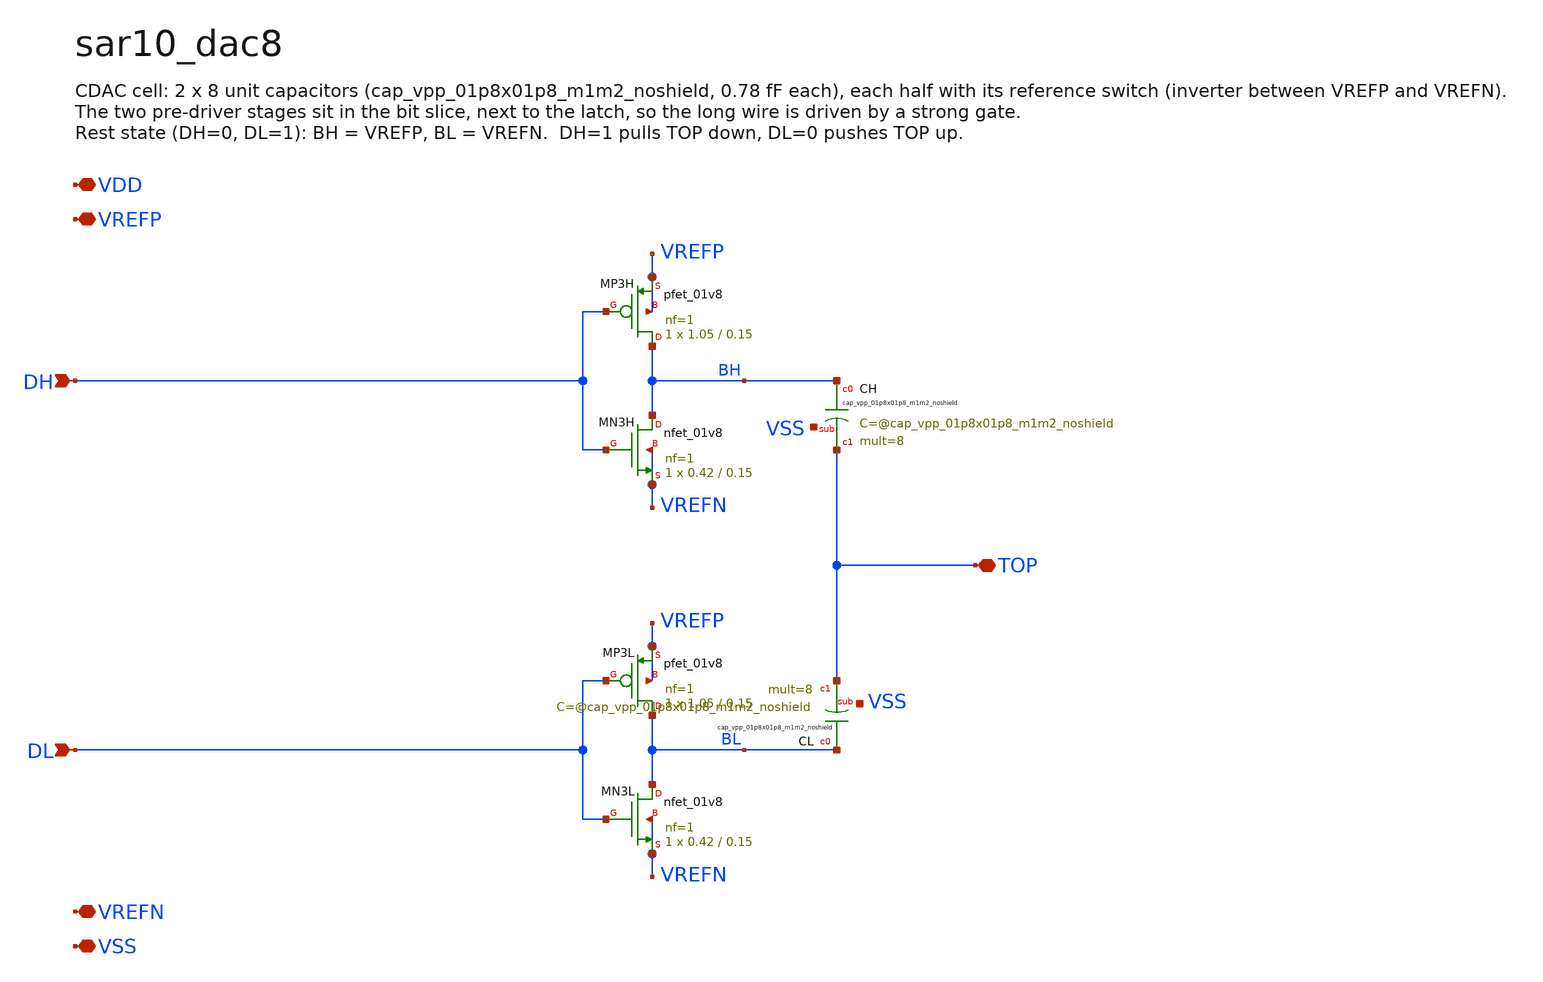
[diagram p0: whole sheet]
** sch_path: xschem/sar10_dac8.sch
**.subckt sar10_dac8 DH DL TOP VDD VREFP VREFN VSS
*.ipin DH
*.ipin DL
*.iopin TOP
*.iopin VDD
*.iopin VREFP
*.iopin VREFN
*.iopin VSS
XMP3H BH DH VREFP VREFP sky130_fd_pr__pfet_01v8 L=0.15 W=1.05 nf=1 ad='int((1 + 1)/2) * 1.05 / 1 * 0.29'
+ as='int((1 + 2)/2) * 1.05 / 1 * 0.29' pd='2*int((1 + 1)/2) * (1.05 / 1 + 0.29)' ps='2*int((1 + 2)/2) * (1.05 / 1 + 0.29)'
+ nrd='0.29 / 1.05 ' nrs='0.29 / 1.05 ' sa=0 sb=0 sd=0 mult=1 m=1
XMN3H BH DH VREFN VREFN sky130_fd_pr__nfet_01v8 L=0.15 W=0.42 nf=1 ad='int((1 + 1)/2) * 0.42 / 1 * 0.29'
+ as='int((1 + 2)/2) * 0.42 / 1 * 0.29' pd='2*int((1 + 1)/2) * (0.42 / 1 + 0.29)' ps='2*int((1 + 2)/2) * (0.42 / 1 + 0.29)'
+ nrd='0.29 / 0.42 ' nrs='0.29 / 0.42 ' sa=0 sb=0 sd=0 mult=1 m=1
XMP3L BL DL VREFP VREFP sky130_fd_pr__pfet_01v8 L=0.15 W=1.05 nf=1 ad='int((1 + 1)/2) * 1.05 / 1 * 0.29'
+ as='int((1 + 2)/2) * 1.05 / 1 * 0.29' pd='2*int((1 + 1)/2) * (1.05 / 1 + 0.29)' ps='2*int((1 + 2)/2) * (1.05 / 1 + 0.29)'
+ nrd='0.29 / 1.05 ' nrs='0.29 / 1.05 ' sa=0 sb=0 sd=0 mult=1 m=1
XMN3L BL DL VREFN VREFN sky130_fd_pr__nfet_01v8 L=0.15 W=0.42 nf=1 ad='int((1 + 1)/2) * 0.42 / 1 * 0.29'
+ as='int((1 + 2)/2) * 0.42 / 1 * 0.29' pd='2*int((1 + 1)/2) * (0.42 / 1 + 0.29)' ps='2*int((1 + 2)/2) * (0.42 / 1 + 0.29)'
+ nrd='0.29 / 0.42 ' nrs='0.29 / 0.42 ' sa=0 sb=0 sd=0 mult=1 m=1
XCH BH TOP VSS sky130_fd_pr__cap_vpp_01p8x01p8_m1m2_noshield mult=8 m=8
XCL BL TOP VSS sky130_fd_pr__cap_vpp_01p8x01p8_m1m2_noshield mult=8 m=8
**.ends
.end
